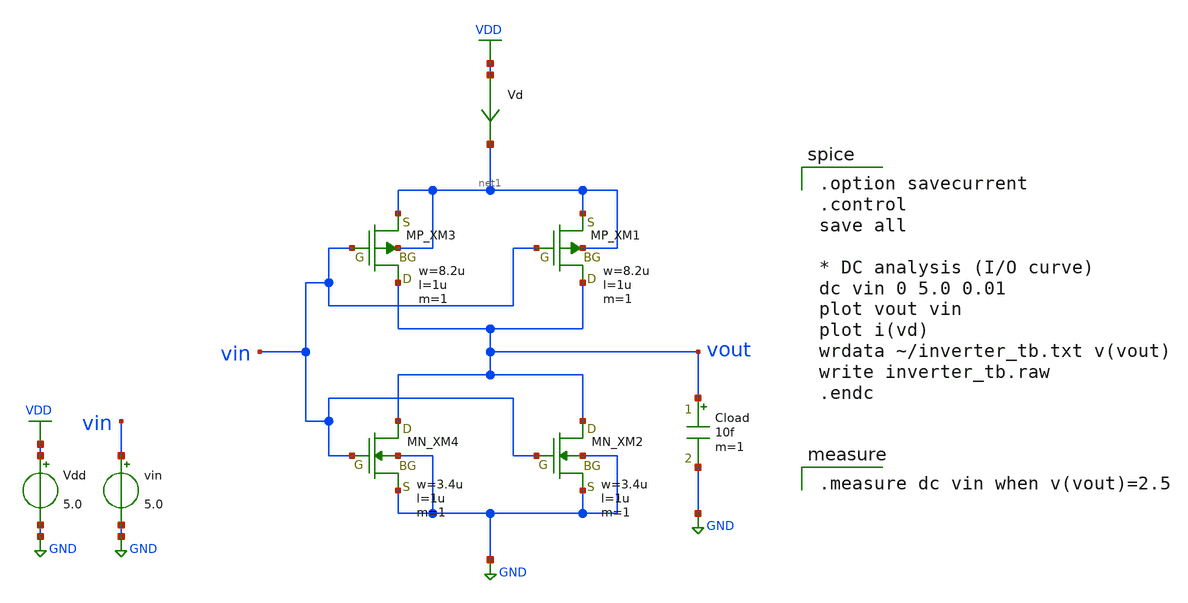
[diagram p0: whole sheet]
** sch_path: member_project/inverter/RISE-A/Talkie_junk/inverter_tb.sch
**.subckt inverter_tb
XXM1 vout vin net1 net1 PMOS w=8.2u l=1u nrd=0 nrs=0 m=1
XXM2 vout vin GND GND NMOS w=3.4u l=1u nrd=0 nrs=0 m=1
XXM3 vout vin net1 net1 PMOS w=8.2u l=1u nrd=0 nrs=0 m=1
XXM4 vout vin GND GND NMOS w=3.4u l=1u nrd=0 nrs=0 m=1
Vdd VDD GND 5.0
vin vin GND 5.0
Vd VDD net1 0
.save i(vd)
Cload vout GND 10f m=1
**** begin user architecture code

.option savecurrent
.control
save all

* DC analysis (I/O curve)
dc vin 0 5.0 0.01
plot vout vin
plot i(vd)
wrdata ~/inverter_tb.txt v(vout)
write inverter_tb.raw
.endc


.measure dc vin when v(vout)=2.5

 .include $::LIB/ip62_models
**** end user architecture code
**.ends
.GLOBAL VDD
.GLOBAL GND
.end
